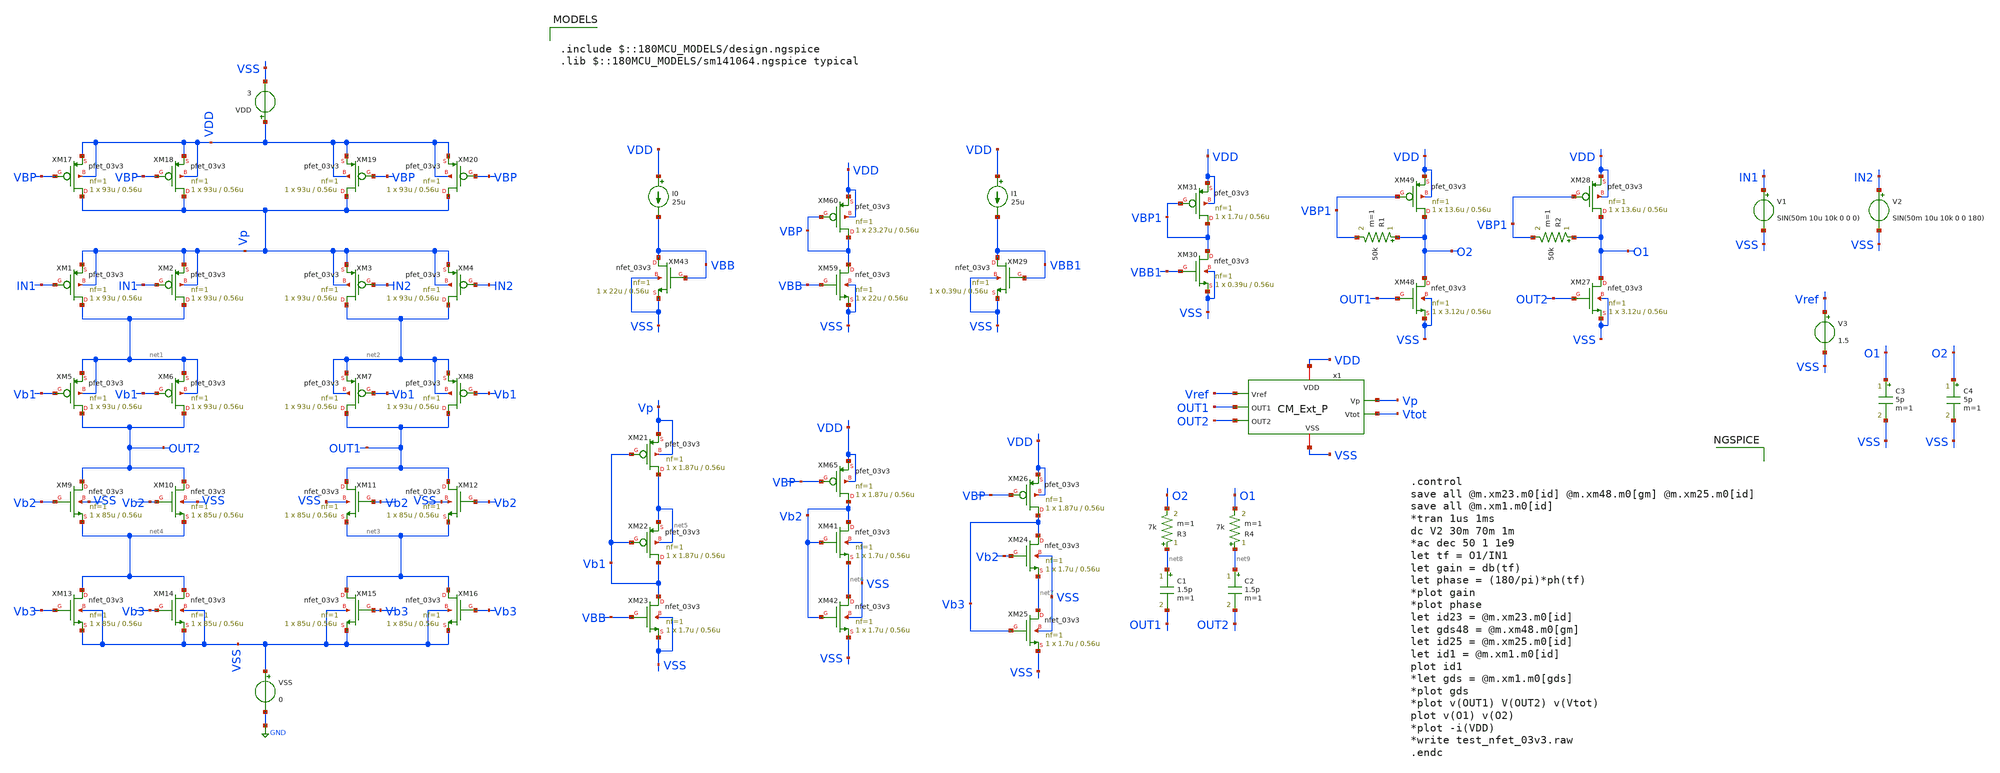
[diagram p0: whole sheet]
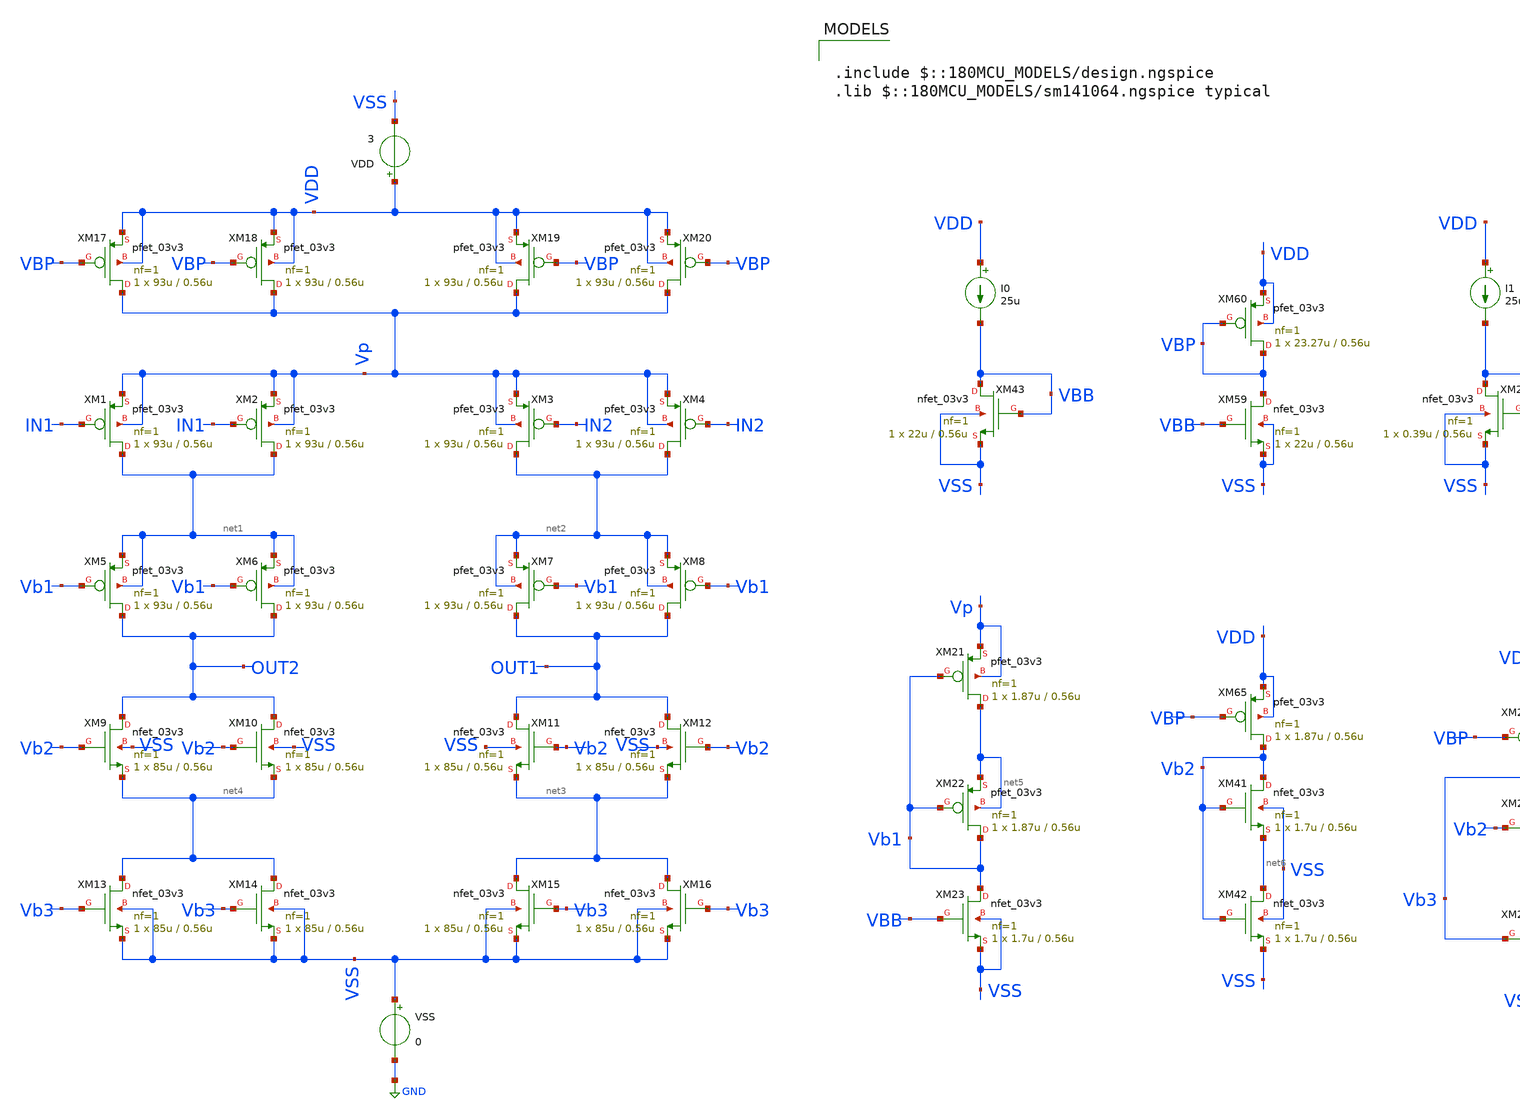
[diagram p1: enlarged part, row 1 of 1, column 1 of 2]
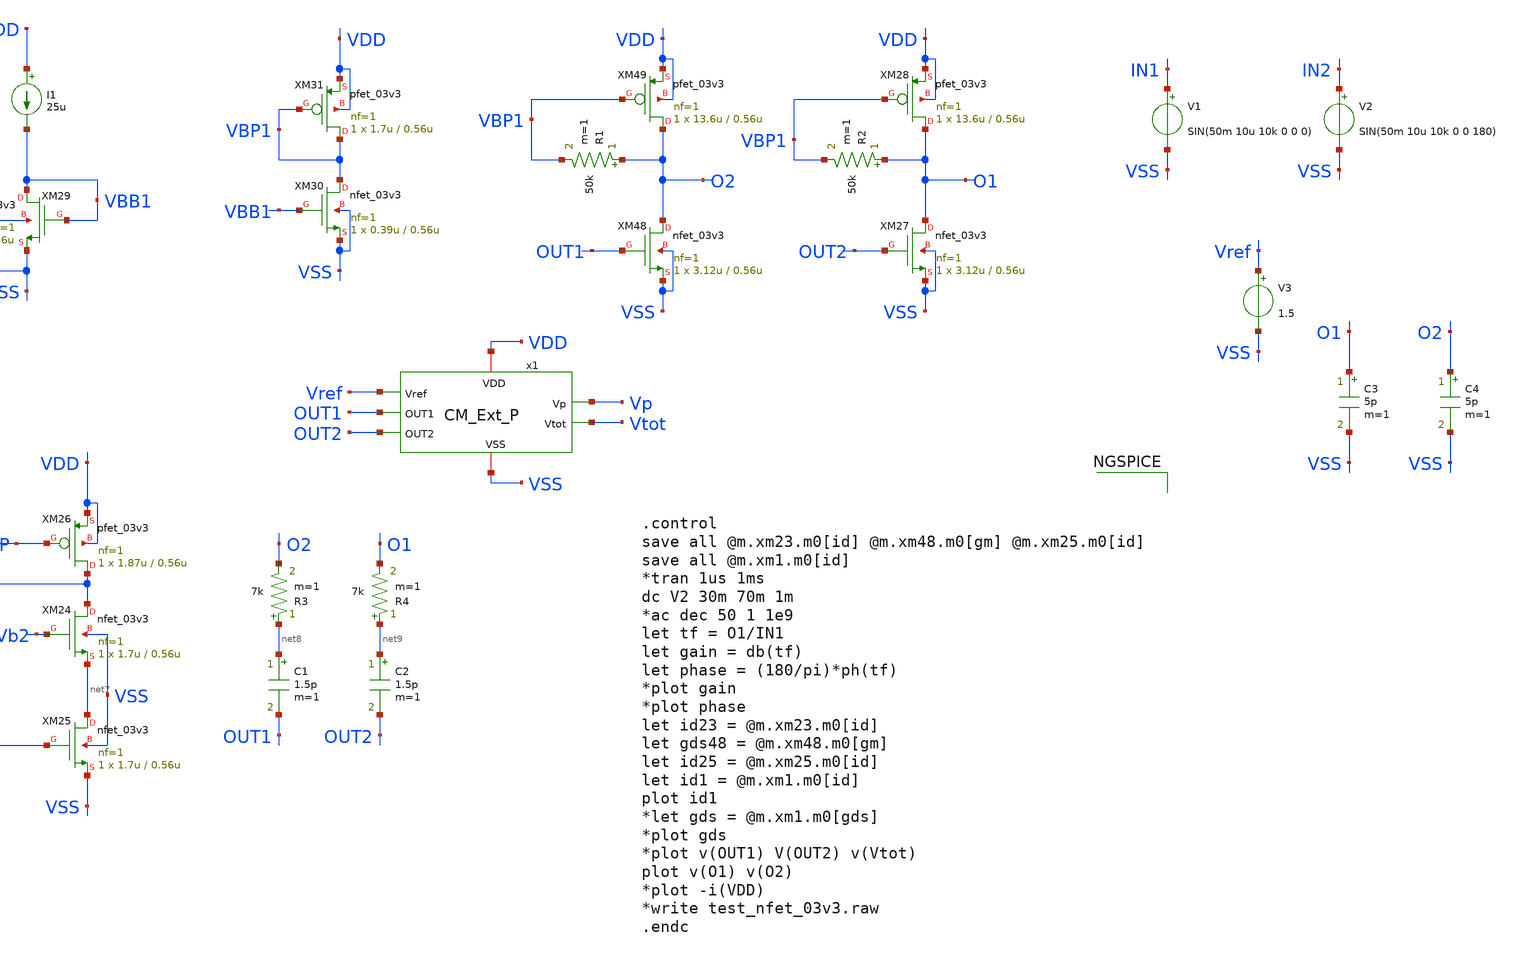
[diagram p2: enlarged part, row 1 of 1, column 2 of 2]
** sch_path: SCOP_INPUT_AND_MUX_PAKISTAN_03/Xschem/Others/PMOS_Op_Amp_1.sch
**.subckt PMOS_Op_Amp_1
XM1 net1 IN1 Vp Vp pfet_03v3 L=0.56u W=93u nf=1 ad='int((nf+1)/2) * W/nf * 0.18u' as='int((nf+2)/2) * W/nf * 0.18u'
+ pd='2*int((nf+1)/2) * (W/nf + 0.18u)' ps='2*int((nf+2)/2) * (W/nf + 0.18u)' nrd='0.18u / W' nrs='0.18u / W'
+ sa=0 sb=0 sd=0 m=1
XM2 net1 IN1 Vp Vp pfet_03v3 L=0.56u W=93u nf=1 ad='int((nf+1)/2) * W/nf * 0.18u' as='int((nf+2)/2) * W/nf * 0.18u'
+ pd='2*int((nf+1)/2) * (W/nf + 0.18u)' ps='2*int((nf+2)/2) * (W/nf + 0.18u)' nrd='0.18u / W' nrs='0.18u / W'
+ sa=0 sb=0 sd=0 m=1
XM3 net2 IN2 Vp Vp pfet_03v3 L=0.56u W=93u nf=1 ad='int((nf+1)/2) * W/nf * 0.18u' as='int((nf+2)/2) * W/nf * 0.18u'
+ pd='2*int((nf+1)/2) * (W/nf + 0.18u)' ps='2*int((nf+2)/2) * (W/nf + 0.18u)' nrd='0.18u / W' nrs='0.18u / W'
+ sa=0 sb=0 sd=0 m=1
XM4 net2 IN2 Vp Vp pfet_03v3 L=0.56u W=93u nf=1 ad='int((nf+1)/2) * W/nf * 0.18u' as='int((nf+2)/2) * W/nf * 0.18u'
+ pd='2*int((nf+1)/2) * (W/nf + 0.18u)' ps='2*int((nf+2)/2) * (W/nf + 0.18u)' nrd='0.18u / W' nrs='0.18u / W'
+ sa=0 sb=0 sd=0 m=1
XM5 OUT2 Vb1 net1 net1 pfet_03v3 L=0.56u W=93u nf=1 ad='int((nf+1)/2) * W/nf * 0.18u' as='int((nf+2)/2) * W/nf * 0.18u'
+ pd='2*int((nf+1)/2) * (W/nf + 0.18u)' ps='2*int((nf+2)/2) * (W/nf + 0.18u)' nrd='0.18u / W' nrs='0.18u / W'
+ sa=0 sb=0 sd=0 m=1
XM6 OUT2 Vb1 net1 net1 pfet_03v3 L=0.56u W=93u nf=1 ad='int((nf+1)/2) * W/nf * 0.18u' as='int((nf+2)/2) * W/nf * 0.18u'
+ pd='2*int((nf+1)/2) * (W/nf + 0.18u)' ps='2*int((nf+2)/2) * (W/nf + 0.18u)' nrd='0.18u / W' nrs='0.18u / W'
+ sa=0 sb=0 sd=0 m=1
XM7 OUT1 Vb1 net2 net2 pfet_03v3 L=0.56u W=93u nf=1 ad='int((nf+1)/2) * W/nf * 0.18u' as='int((nf+2)/2) * W/nf * 0.18u'
+ pd='2*int((nf+1)/2) * (W/nf + 0.18u)' ps='2*int((nf+2)/2) * (W/nf + 0.18u)' nrd='0.18u / W' nrs='0.18u / W'
+ sa=0 sb=0 sd=0 m=1
XM8 OUT1 Vb1 net2 net2 pfet_03v3 L=0.56u W=93u nf=1 ad='int((nf+1)/2) * W/nf * 0.18u' as='int((nf+2)/2) * W/nf * 0.18u'
+ pd='2*int((nf+1)/2) * (W/nf + 0.18u)' ps='2*int((nf+2)/2) * (W/nf + 0.18u)' nrd='0.18u / W' nrs='0.18u / W'
+ sa=0 sb=0 sd=0 m=1
XM9 OUT2 Vb2 net4 VSS nfet_03v3 L=0.56u W=85u nf=1 ad='int((nf+1)/2) * W/nf * 0.18u' as='int((nf+2)/2) * W/nf * 0.18u'
+ pd='2*int((nf+1)/2) * (W/nf + 0.18u)' ps='2*int((nf+2)/2) * (W/nf + 0.18u)' nrd='0.18u / W' nrs='0.18u / W'
+ sa=0 sb=0 sd=0 m=1
XM10 OUT2 Vb2 net4 VSS nfet_03v3 L=0.56u W=85u nf=1 ad='int((nf+1)/2) * W/nf * 0.18u' as='int((nf+2)/2) * W/nf * 0.18u'
+ pd='2*int((nf+1)/2) * (W/nf + 0.18u)' ps='2*int((nf+2)/2) * (W/nf + 0.18u)' nrd='0.18u / W' nrs='0.18u / W'
+ sa=0 sb=0 sd=0 m=1
XM11 OUT1 Vb2 net3 VSS nfet_03v3 L=0.56u W=85u nf=1 ad='int((nf+1)/2) * W/nf * 0.18u' as='int((nf+2)/2) * W/nf * 0.18u'
+ pd='2*int((nf+1)/2) * (W/nf + 0.18u)' ps='2*int((nf+2)/2) * (W/nf + 0.18u)' nrd='0.18u / W' nrs='0.18u / W'
+ sa=0 sb=0 sd=0 m=1
XM12 OUT1 Vb2 net3 VSS nfet_03v3 L=0.56u W=85u nf=1 ad='int((nf+1)/2) * W/nf * 0.18u' as='int((nf+2)/2) * W/nf * 0.18u'
+ pd='2*int((nf+1)/2) * (W/nf + 0.18u)' ps='2*int((nf+2)/2) * (W/nf + 0.18u)' nrd='0.18u / W' nrs='0.18u / W'
+ sa=0 sb=0 sd=0 m=1
XM13 net4 Vb3 VSS VSS nfet_03v3 L=0.56u W=85u nf=1 ad='int((nf+1)/2) * W/nf * 0.18u' as='int((nf+2)/2) * W/nf * 0.18u'
+ pd='2*int((nf+1)/2) * (W/nf + 0.18u)' ps='2*int((nf+2)/2) * (W/nf + 0.18u)' nrd='0.18u / W' nrs='0.18u / W'
+ sa=0 sb=0 sd=0 m=1
XM14 net4 Vb3 VSS VSS nfet_03v3 L=0.56u W=85u nf=1 ad='int((nf+1)/2) * W/nf * 0.18u' as='int((nf+2)/2) * W/nf * 0.18u'
+ pd='2*int((nf+1)/2) * (W/nf + 0.18u)' ps='2*int((nf+2)/2) * (W/nf + 0.18u)' nrd='0.18u / W' nrs='0.18u / W'
+ sa=0 sb=0 sd=0 m=1
XM15 net3 Vb3 VSS VSS nfet_03v3 L=0.56u W=85u nf=1 ad='int((nf+1)/2) * W/nf * 0.18u' as='int((nf+2)/2) * W/nf * 0.18u'
+ pd='2*int((nf+1)/2) * (W/nf + 0.18u)' ps='2*int((nf+2)/2) * (W/nf + 0.18u)' nrd='0.18u / W' nrs='0.18u / W'
+ sa=0 sb=0 sd=0 m=1
XM16 net3 Vb3 VSS VSS nfet_03v3 L=0.56u W=85u nf=1 ad='int((nf+1)/2) * W/nf * 0.18u' as='int((nf+2)/2) * W/nf * 0.18u'
+ pd='2*int((nf+1)/2) * (W/nf + 0.18u)' ps='2*int((nf+2)/2) * (W/nf + 0.18u)' nrd='0.18u / W' nrs='0.18u / W'
+ sa=0 sb=0 sd=0 m=1
XM17 Vp VBP VDD VDD pfet_03v3 L=0.56u W=93u nf=1 ad='int((nf+1)/2) * W/nf * 0.18u' as='int((nf+2)/2) * W/nf * 0.18u'
+ pd='2*int((nf+1)/2) * (W/nf + 0.18u)' ps='2*int((nf+2)/2) * (W/nf + 0.18u)' nrd='0.18u / W' nrs='0.18u / W'
+ sa=0 sb=0 sd=0 m=1
XM18 Vp VBP VDD VDD pfet_03v3 L=0.56u W=93u nf=1 ad='int((nf+1)/2) * W/nf * 0.18u' as='int((nf+2)/2) * W/nf * 0.18u'
+ pd='2*int((nf+1)/2) * (W/nf + 0.18u)' ps='2*int((nf+2)/2) * (W/nf + 0.18u)' nrd='0.18u / W' nrs='0.18u / W'
+ sa=0 sb=0 sd=0 m=1
XM19 Vp VBP VDD VDD pfet_03v3 L=0.56u W=93u nf=1 ad='int((nf+1)/2) * W/nf * 0.18u' as='int((nf+2)/2) * W/nf * 0.18u'
+ pd='2*int((nf+1)/2) * (W/nf + 0.18u)' ps='2*int((nf+2)/2) * (W/nf + 0.18u)' nrd='0.18u / W' nrs='0.18u / W'
+ sa=0 sb=0 sd=0 m=1
XM20 Vp VBP VDD VDD pfet_03v3 L=0.56u W=93u nf=1 ad='int((nf+1)/2) * W/nf * 0.18u' as='int((nf+2)/2) * W/nf * 0.18u'
+ pd='2*int((nf+1)/2) * (W/nf + 0.18u)' ps='2*int((nf+2)/2) * (W/nf + 0.18u)' nrd='0.18u / W' nrs='0.18u / W'
+ sa=0 sb=0 sd=0 m=1
VSS VSS GND 0
VDD VDD VSS 3
XM43 VBB VBB VSS VSS nfet_03v3 L=0.56u W=22u nf=1 ad='int((nf+1)/2) * W/nf * 0.18u' as='int((nf+2)/2) * W/nf * 0.18u'
+ pd='2*int((nf+1)/2) * (W/nf + 0.18u)' ps='2*int((nf+2)/2) * (W/nf + 0.18u)' nrd='0.18u / W' nrs='0.18u / W'
+ sa=0 sb=0 sd=0 m=1
I0 VDD VBB 25u
XM59 VBP VBB VSS VSS nfet_03v3 L=0.56u W=22u nf=1 ad='int((nf+1)/2) * W/nf * 0.18u' as='int((nf+2)/2) * W/nf * 0.18u'
+ pd='2*int((nf+1)/2) * (W/nf + 0.18u)' ps='2*int((nf+2)/2) * (W/nf + 0.18u)' nrd='0.18u / W' nrs='0.18u / W'
+ sa=0 sb=0 sd=0 m=1
XM60 VBP VBP VDD VDD pfet_03v3 L=0.56u W=23.27u nf=1 ad='int((nf+1)/2) * W/nf * 0.18u' as='int((nf+2)/2) * W/nf * 0.18u'
+ pd='2*int((nf+1)/2) * (W/nf + 0.18u)' ps='2*int((nf+2)/2) * (W/nf + 0.18u)' nrd='0.18u / W' nrs='0.18u / W'
+ sa=0 sb=0 sd=0 m=1
XM21 net5 Vb1 Vp Vp pfet_03v3 L=0.56u W=1.87u nf=1 ad='int((nf+1)/2) * W/nf * 0.18u' as='int((nf+2)/2) * W/nf * 0.18u'
+ pd='2*int((nf+1)/2) * (W/nf + 0.18u)' ps='2*int((nf+2)/2) * (W/nf + 0.18u)' nrd='0.18u / W' nrs='0.18u / W'
+ sa=0 sb=0 sd=0 m=1
XM22 Vb1 Vb1 net5 net5 pfet_03v3 L=0.56u W=1.87u nf=1 ad='int((nf+1)/2) * W/nf * 0.18u' as='int((nf+2)/2) * W/nf * 0.18u'
+ pd='2*int((nf+1)/2) * (W/nf + 0.18u)' ps='2*int((nf+2)/2) * (W/nf + 0.18u)' nrd='0.18u / W' nrs='0.18u / W'
+ sa=0 sb=0 sd=0 m=1
XM23 Vb1 VBB VSS VSS nfet_03v3 L=0.56u W=1.7u nf=1 ad='int((nf+1)/2) * W/nf * 0.18u' as='int((nf+2)/2) * W/nf * 0.18u'
+ pd='2*int((nf+1)/2) * (W/nf + 0.18u)' ps='2*int((nf+2)/2) * (W/nf + 0.18u)' nrd='0.18u / W' nrs='0.18u / W'
+ sa=0 sb=0 sd=0 m=1
XM41 Vb2 Vb2 net6 VSS nfet_03v3 L=0.56u W=1.7u nf=1 ad='int((nf+1)/2) * W/nf * 0.18u' as='int((nf+2)/2) * W/nf * 0.18u'
+ pd='2*int((nf+1)/2) * (W/nf + 0.18u)' ps='2*int((nf+2)/2) * (W/nf + 0.18u)' nrd='0.18u / W' nrs='0.18u / W'
+ sa=0 sb=0 sd=0 m=1
XM42 net6 Vb2 VSS VSS nfet_03v3 L=0.56u W=1.7u nf=1 ad='int((nf+1)/2) * W/nf * 0.18u' as='int((nf+2)/2) * W/nf * 0.18u'
+ pd='2*int((nf+1)/2) * (W/nf + 0.18u)' ps='2*int((nf+2)/2) * (W/nf + 0.18u)' nrd='0.18u / W' nrs='0.18u / W'
+ sa=0 sb=0 sd=0 m=1
XM65 Vb2 VBP VDD VDD pfet_03v3 L=0.56u W=1.87u nf=1 ad='int((nf+1)/2) * W/nf * 0.18u' as='int((nf+2)/2) * W/nf * 0.18u'
+ pd='2*int((nf+1)/2) * (W/nf + 0.18u)' ps='2*int((nf+2)/2) * (W/nf + 0.18u)' nrd='0.18u / W' nrs='0.18u / W'
+ sa=0 sb=0 sd=0 m=1
XM24 Vb3 Vb2 net7 VSS nfet_03v3 L=0.56u W=1.7u nf=1 ad='int((nf+1)/2) * W/nf * 0.18u' as='int((nf+2)/2) * W/nf * 0.18u'
+ pd='2*int((nf+1)/2) * (W/nf + 0.18u)' ps='2*int((nf+2)/2) * (W/nf + 0.18u)' nrd='0.18u / W' nrs='0.18u / W'
+ sa=0 sb=0 sd=0 m=1
XM25 net7 Vb3 VSS VSS nfet_03v3 L=0.56u W=1.7u nf=1 ad='int((nf+1)/2) * W/nf * 0.18u' as='int((nf+2)/2) * W/nf * 0.18u'
+ pd='2*int((nf+1)/2) * (W/nf + 0.18u)' ps='2*int((nf+2)/2) * (W/nf + 0.18u)' nrd='0.18u / W' nrs='0.18u / W'
+ sa=0 sb=0 sd=0 m=1
XM26 Vb3 VBP VDD VDD pfet_03v3 L=0.56u W=1.87u nf=1 ad='int((nf+1)/2) * W/nf * 0.18u' as='int((nf+2)/2) * W/nf * 0.18u'
+ pd='2*int((nf+1)/2) * (W/nf + 0.18u)' ps='2*int((nf+2)/2) * (W/nf + 0.18u)' nrd='0.18u / W' nrs='0.18u / W'
+ sa=0 sb=0 sd=0 m=1
x1 Vref Vp Vtot VDD OUT1 VSS OUT2 CM_Ext_P
XM48 O2 OUT1 VSS VSS nfet_03v3 L=0.56u W=3.12u nf=1 ad='int((nf+1)/2) * W/nf * 0.18u' as='int((nf+2)/2) * W/nf * 0.18u'
+ pd='2*int((nf+1)/2) * (W/nf + 0.18u)' ps='2*int((nf+2)/2) * (W/nf + 0.18u)' nrd='0.18u / W' nrs='0.18u / W'
+ sa=0 sb=0 sd=0 m=1
XM49 O2 VBP1 VDD VDD pfet_03v3 L=0.56u W=13.6u nf=1 ad='int((nf+1)/2) * W/nf * 0.18u' as='int((nf+2)/2) * W/nf * 0.18u'
+ pd='2*int((nf+1)/2) * (W/nf + 0.18u)' ps='2*int((nf+2)/2) * (W/nf + 0.18u)' nrd='0.18u / W' nrs='0.18u / W'
+ sa=0 sb=0 sd=0 m=1
XM27 O1 OUT2 VSS VSS nfet_03v3 L=0.56u W=3.12u nf=1 ad='int((nf+1)/2) * W/nf * 0.18u' as='int((nf+2)/2) * W/nf * 0.18u'
+ pd='2*int((nf+1)/2) * (W/nf + 0.18u)' ps='2*int((nf+2)/2) * (W/nf + 0.18u)' nrd='0.18u / W' nrs='0.18u / W'
+ sa=0 sb=0 sd=0 m=1
XM28 O1 VBP1 VDD VDD pfet_03v3 L=0.56u W=13.6u nf=1 ad='int((nf+1)/2) * W/nf * 0.18u' as='int((nf+2)/2) * W/nf * 0.18u'
+ pd='2*int((nf+1)/2) * (W/nf + 0.18u)' ps='2*int((nf+2)/2) * (W/nf + 0.18u)' nrd='0.18u / W' nrs='0.18u / W'
+ sa=0 sb=0 sd=0 m=1
XM29 VBB1 VBB1 VSS VSS nfet_03v3 L=0.56u W=0.39u nf=1 ad='int((nf+1)/2) * W/nf * 0.18u' as='int((nf+2)/2) * W/nf * 0.18u'
+ pd='2*int((nf+1)/2) * (W/nf + 0.18u)' ps='2*int((nf+2)/2) * (W/nf + 0.18u)' nrd='0.18u / W' nrs='0.18u / W'
+ sa=0 sb=0 sd=0 m=1
I1 VDD VBB1 25u
XM30 VBP1 VBB1 VSS VSS nfet_03v3 L=0.56u W=0.39u nf=1 ad='int((nf+1)/2) * W/nf * 0.18u' as='int((nf+2)/2) * W/nf * 0.18u'
+ pd='2*int((nf+1)/2) * (W/nf + 0.18u)' ps='2*int((nf+2)/2) * (W/nf + 0.18u)' nrd='0.18u / W' nrs='0.18u / W'
+ sa=0 sb=0 sd=0 m=1
XM31 VBP1 VBP1 VDD VDD pfet_03v3 L=0.56u W=1.7u nf=1 ad='int((nf+1)/2) * W/nf * 0.18u' as='int((nf+2)/2) * W/nf * 0.18u'
+ pd='2*int((nf+1)/2) * (W/nf + 0.18u)' ps='2*int((nf+2)/2) * (W/nf + 0.18u)' nrd='0.18u / W' nrs='0.18u / W'
+ sa=0 sb=0 sd=0 m=1
R1 O2 VBP1 50k m=1
R2 O1 VBP1 50k m=1
C1 net8 OUT1 1.5p m=1
C2 net9 OUT2 1.5p m=1
V1 IN1 VSS SIN(50m 10u 10k 0 0 0)
V2 IN2 VSS SIN(50m 10u 10k 0 0 180)
V3 Vref VSS 1.5
C3 O1 VSS 5p m=1
C4 O2 VSS 5p m=1
R3 net8 O2 7k m=1
R4 net9 O1 7k m=1
**** begin user architecture code

.include $::180MCU_MODELS/design.ngspice
.lib $::180MCU_MODELS/sm141064.ngspice typical




.control
save all @m.xm23.m0[id] @m.xm48.m0[gm] @m.xm25.m0[id]
save all @m.xm1.m0[id]
*tran 1us 1ms
dc V2 30m 70m 1m
*ac dec 50 1 1e9
let tf = O1/IN1
let gain = db(tf)
let phase = (180/pi)*ph(tf)
*plot gain
*plot phase
let id23 = @m.xm23.m0[id]
let gds48 = @m.xm48.m0[gm]
let id25 = @m.xm25.m0[id]
let id1 = @m.xm1.m0[id]
plot id1
*let gds = @m.xm1.m0[gds]
*plot gds
*plot v(OUT1) V(OUT2) v(Vtot)
plot v(O1) v(O2)
*plot -i(VDD)
*write test_nfet_03v3.raw
.endc


**** end user architecture code
**.ends

* expanding   symbol:  Tapeout/CM_Ext_P.sym # of pins=7
** sym_path: SCOP_INPUT_AND_MUX_PAKISTAN_03/Xschem/Others/CM_Ext_P.sym
** sch_path: SCOP_INPUT_AND_MUX_PAKISTAN_03/Xschem/Others/CM_Ext_P.sch
.subckt CM_Ext_P Vref Vp Vtot VDD OUT1 VSS OUT2
*.ipin Vref
*.ipin OUT1
*.ipin OUT2
*.opin Vp
*.iopin VDD
*.iopin VSS
*.opin Vtot
R2 Vtot VB 100k m=1
R1 Vtot VA 100k m=1
R4 VD Vtot 100k m=1
R3 VC Vtot 100k m=1
XM50 VSS OUT2 VC VC pfet_03v3 L=0.56u W=9.35u nf=1 ad='int((nf+1)/2) * W/nf * 0.18u' as='int((nf+2)/2) * W/nf * 0.18u'
+ pd='2*int((nf+1)/2) * (W/nf + 0.18u)' ps='2*int((nf+2)/2) * (W/nf + 0.18u)' nrd='0.18u / W' nrs='0.18u / W'
+ sa=0 sb=0 sd=0 m=1
XM51 VSS OUT1 VD VD pfet_03v3 L=0.56u W=9.35u nf=1 ad='int((nf+1)/2) * W/nf * 0.18u' as='int((nf+2)/2) * W/nf * 0.18u'
+ pd='2*int((nf+1)/2) * (W/nf + 0.18u)' ps='2*int((nf+2)/2) * (W/nf + 0.18u)' nrd='0.18u / W' nrs='0.18u / W'
+ sa=0 sb=0 sd=0 m=1
XM61 VD VBP VDD VDD pfet_03v3 L=0.56u W=9.35u nf=1 ad='int((nf+1)/2) * W/nf * 0.18u' as='int((nf+2)/2) * W/nf * 0.18u'
+ pd='2*int((nf+1)/2) * (W/nf + 0.18u)' ps='2*int((nf+2)/2) * (W/nf + 0.18u)' nrd='0.18u / W' nrs='0.18u / W'
+ sa=0 sb=0 sd=0 m=1
XM62 VC VBP VDD VDD pfet_03v3 L=0.56u W=9.35u nf=1 ad='int((nf+1)/2) * W/nf * 0.18u' as='int((nf+2)/2) * W/nf * 0.18u'
+ pd='2*int((nf+1)/2) * (W/nf + 0.18u)' ps='2*int((nf+2)/2) * (W/nf + 0.18u)' nrd='0.18u / W' nrs='0.18u / W'
+ sa=0 sb=0 sd=0 m=1
XM59 VBP VBB VSS VSS nfet_03v3 L=0.56u W=8.8u nf=1 ad='int((nf+1)/2) * W/nf * 0.18u' as='int((nf+2)/2) * W/nf * 0.18u'
+ pd='2*int((nf+1)/2) * (W/nf + 0.18u)' ps='2*int((nf+2)/2) * (W/nf + 0.18u)' nrd='0.18u / W' nrs='0.18u / W'
+ sa=0 sb=0 sd=0 m=1
XM60 VBP VBP VDD VDD pfet_03v3 L=0.56u W=9.35u nf=1 ad='int((nf+1)/2) * W/nf * 0.18u' as='int((nf+2)/2) * W/nf * 0.18u'
+ pd='2*int((nf+1)/2) * (W/nf + 0.18u)' ps='2*int((nf+2)/2) * (W/nf + 0.18u)' nrd='0.18u / W' nrs='0.18u / W'
+ sa=0 sb=0 sd=0 m=1
XM49 VDD OUT1 VB VSS nfet_03v3 L=0.56u W=8.8u nf=1 ad='int((nf+1)/2) * W/nf * 0.18u' as='int((nf+2)/2) * W/nf * 0.18u'
+ pd='2*int((nf+1)/2) * (W/nf + 0.18u)' ps='2*int((nf+2)/2) * (W/nf + 0.18u)' nrd='0.18u / W' nrs='0.18u / W'
+ sa=0 sb=0 sd=0 m=1
XM58 VB VBB VSS VSS nfet_03v3 L=0.56u W=8.8u nf=1 ad='int((nf+1)/2) * W/nf * 0.18u' as='int((nf+2)/2) * W/nf * 0.18u'
+ pd='2*int((nf+1)/2) * (W/nf + 0.18u)' ps='2*int((nf+2)/2) * (W/nf + 0.18u)' nrd='0.18u / W' nrs='0.18u / W'
+ sa=0 sb=0 sd=0 m=1
XM48 VDD OUT2 VA VSS nfet_03v3 L=0.56u W=8.8u nf=1 ad='int((nf+1)/2) * W/nf * 0.18u' as='int((nf+2)/2) * W/nf * 0.18u'
+ pd='2*int((nf+1)/2) * (W/nf + 0.18u)' ps='2*int((nf+2)/2) * (W/nf + 0.18u)' nrd='0.18u / W' nrs='0.18u / W'
+ sa=0 sb=0 sd=0 m=1
XM57 VA VBB VSS VSS nfet_03v3 L=0.56u W=8.8u nf=1 ad='int((nf+1)/2) * W/nf * 0.18u' as='int((nf+2)/2) * W/nf * 0.18u'
+ pd='2*int((nf+1)/2) * (W/nf + 0.18u)' ps='2*int((nf+2)/2) * (W/nf + 0.18u)' nrd='0.18u / W' nrs='0.18u / W'
+ sa=0 sb=0 sd=0 m=1
XM43 VBB VBB VSS VSS nfet_03v3 L=0.56u W=22u nf=1 ad='int((nf+1)/2) * W/nf * 0.18u' as='int((nf+2)/2) * W/nf * 0.18u'
+ pd='2*int((nf+1)/2) * (W/nf + 0.18u)' ps='2*int((nf+2)/2) * (W/nf + 0.18u)' nrd='0.18u / W' nrs='0.18u / W'
+ sa=0 sb=0 sd=0 m=1
I0 VDD VBB 25u
XM1 net1 net1 VDD VDD pfet_03v3 L=0.56u W=23.4u nf=1 ad='int((nf+1)/2) * W/nf * 0.18u' as='int((nf+2)/2) * W/nf * 0.18u'
+ pd='2*int((nf+1)/2) * (W/nf + 0.18u)' ps='2*int((nf+2)/2) * (W/nf + 0.18u)' nrd='0.18u / W' nrs='0.18u / W'
+ sa=0 sb=0 sd=0 m=1
XM2 net2 net1 VDD VDD pfet_03v3 L=0.56u W=23.4u nf=1 ad='int((nf+1)/2) * W/nf * 0.18u' as='int((nf+2)/2) * W/nf * 0.18u'
+ pd='2*int((nf+1)/2) * (W/nf + 0.18u)' ps='2*int((nf+2)/2) * (W/nf + 0.18u)' nrd='0.18u / W' nrs='0.18u / W'
+ sa=0 sb=0 sd=0 m=1
XM3 net1 Vtot net3 VSS nfet_03v3 L=0.56u W=22u nf=1 ad='int((nf+1)/2) * W/nf * 0.18u' as='int((nf+2)/2) * W/nf * 0.18u'
+ pd='2*int((nf+1)/2) * (W/nf + 0.18u)' ps='2*int((nf+2)/2) * (W/nf + 0.18u)' nrd='0.18u / W' nrs='0.18u / W'
+ sa=0 sb=0 sd=0 m=1
XM4 net2 Vref net3 VSS nfet_03v3 L=0.56u W=22u nf=1 ad='int((nf+1)/2) * W/nf * 0.18u' as='int((nf+2)/2) * W/nf * 0.18u'
+ pd='2*int((nf+1)/2) * (W/nf + 0.18u)' ps='2*int((nf+2)/2) * (W/nf + 0.18u)' nrd='0.18u / W' nrs='0.18u / W'
+ sa=0 sb=0 sd=0 m=1
XM5 net3 VBB VSS VSS nfet_03v3 L=0.56u W=22u nf=1 ad='int((nf+1)/2) * W/nf * 0.18u' as='int((nf+2)/2) * W/nf * 0.18u'
+ pd='2*int((nf+1)/2) * (W/nf + 0.18u)' ps='2*int((nf+2)/2) * (W/nf + 0.18u)' nrd='0.18u / W' nrs='0.18u / W'
+ sa=0 sb=0 sd=0 m=1
XM6 Vp net2 VDD VDD pfet_03v3 L=0.56u W=23.4u nf=1 ad='int((nf+1)/2) * W/nf * 0.18u' as='int((nf+2)/2) * W/nf * 0.18u'
+ pd='2*int((nf+1)/2) * (W/nf + 0.18u)' ps='2*int((nf+2)/2) * (W/nf + 0.18u)' nrd='0.18u / W' nrs='0.18u / W'
+ sa=0 sb=0 sd=0 m=1
.ends

.GLOBAL GND
.end
